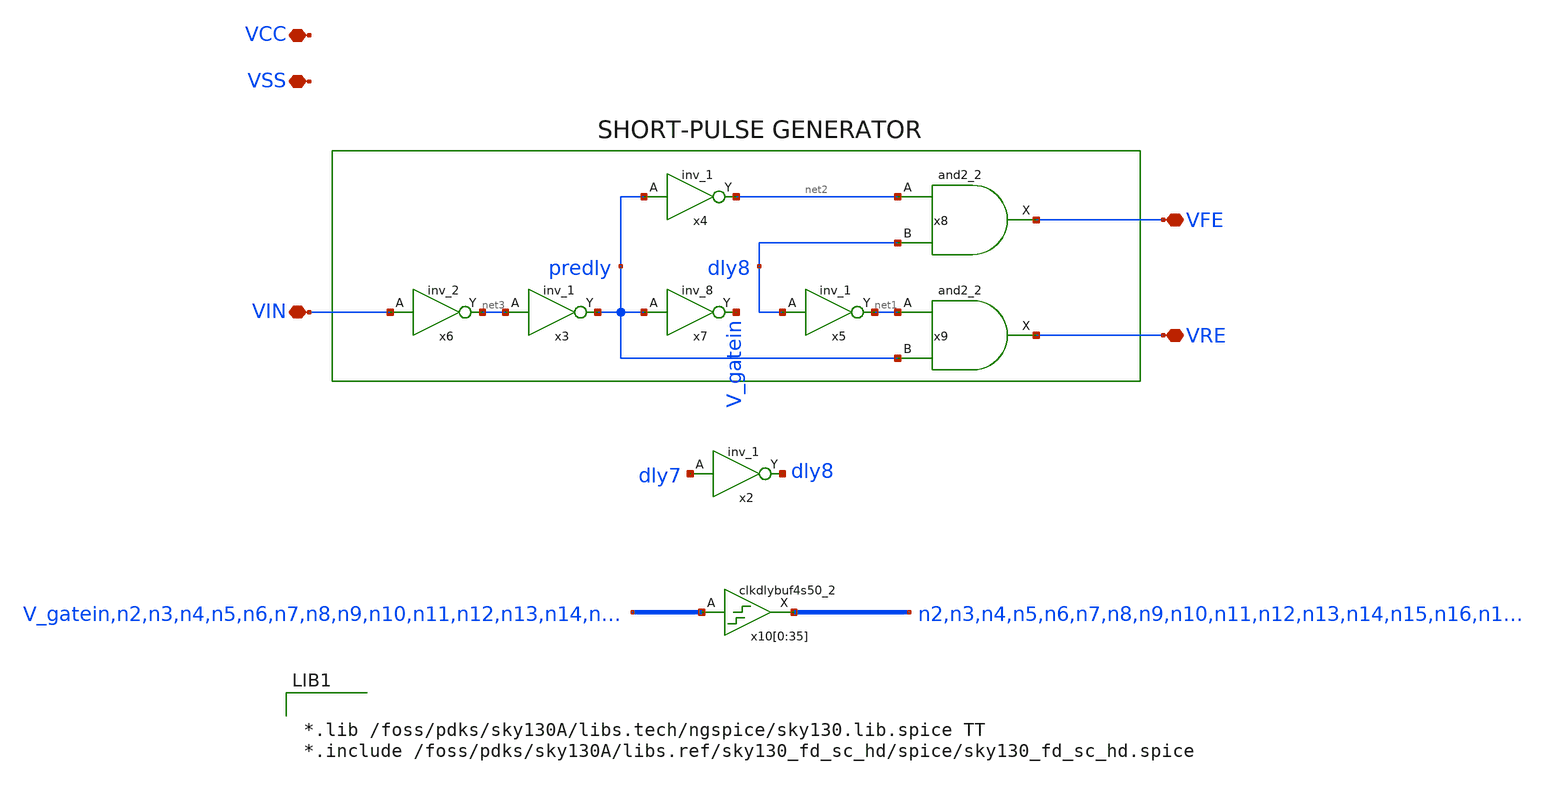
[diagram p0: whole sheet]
** sch_path: xschem/short_pulse_generator.sch
**.subckt short_pulse_generator VIN VFE VRE VCC VSS
*.iopin VIN
*.iopin VFE
*.iopin VRE
*.iopin VCC
*.iopin VSS
x3 net3 VSS VSS VCC VCC predly sky130_fd_sc_hd__inv_1
x4 predly VSS VSS VCC VCC net2 sky130_fd_sc_hd__inv_1
x5 dly8 VSS VSS VCC VCC net1 sky130_fd_sc_hd__inv_1
x6 VIN VSS VSS VCC VCC net3 sky130_fd_sc_hd__inv_2
x7 predly VSS VSS VCC VCC V_gatein sky130_fd_sc_hd__inv_8
x8 net2 dly8 VSS VSS VCC VCC VFE sky130_fd_sc_hd__and2_2
x9 net1 predly VSS VSS VCC VCC VRE sky130_fd_sc_hd__and2_2
x2 dly7 VSS VSS VCC VCC dly8 sky130_fd_sc_hd__inv_1
x10[0] V_gatein VSS VSS VCC VCC n2 sky130_fd_sc_hd__clkdlybuf4s50_2
x10[1] n2 VSS VSS VCC VCC n3 sky130_fd_sc_hd__clkdlybuf4s50_2
x10[2] n3 VSS VSS VCC VCC n4 sky130_fd_sc_hd__clkdlybuf4s50_2
x10[3] n4 VSS VSS VCC VCC n5 sky130_fd_sc_hd__clkdlybuf4s50_2
x10[4] n5 VSS VSS VCC VCC n6 sky130_fd_sc_hd__clkdlybuf4s50_2
x10[5] n6 VSS VSS VCC VCC n7 sky130_fd_sc_hd__clkdlybuf4s50_2
x10[6] n7 VSS VSS VCC VCC n8 sky130_fd_sc_hd__clkdlybuf4s50_2
x10[7] n8 VSS VSS VCC VCC n9 sky130_fd_sc_hd__clkdlybuf4s50_2
x10[8] n9 VSS VSS VCC VCC n10 sky130_fd_sc_hd__clkdlybuf4s50_2
x10[9] n10 VSS VSS VCC VCC n11 sky130_fd_sc_hd__clkdlybuf4s50_2
x10[10] n11 VSS VSS VCC VCC n12 sky130_fd_sc_hd__clkdlybuf4s50_2
x10[11] n12 VSS VSS VCC VCC n13 sky130_fd_sc_hd__clkdlybuf4s50_2
x10[12] n13 VSS VSS VCC VCC n14 sky130_fd_sc_hd__clkdlybuf4s50_2
x10[13] n14 VSS VSS VCC VCC n15 sky130_fd_sc_hd__clkdlybuf4s50_2
x10[14] n15 VSS VSS VCC VCC n16 sky130_fd_sc_hd__clkdlybuf4s50_2
x10[15] n16 VSS VSS VCC VCC n17 sky130_fd_sc_hd__clkdlybuf4s50_2
x10[16] n17 VSS VSS VCC VCC n18 sky130_fd_sc_hd__clkdlybuf4s50_2
x10[17] n18 VSS VSS VCC VCC n19 sky130_fd_sc_hd__clkdlybuf4s50_2
x10[18] n19 VSS VSS VCC VCC n20 sky130_fd_sc_hd__clkdlybuf4s50_2
x10[19] n20 VSS VSS VCC VCC n21 sky130_fd_sc_hd__clkdlybuf4s50_2
x10[20] n21 VSS VSS VCC VCC n22 sky130_fd_sc_hd__clkdlybuf4s50_2
x10[21] n22 VSS VSS VCC VCC n23 sky130_fd_sc_hd__clkdlybuf4s50_2
x10[22] n23 VSS VSS VCC VCC n24 sky130_fd_sc_hd__clkdlybuf4s50_2
x10[23] n24 VSS VSS VCC VCC n25 sky130_fd_sc_hd__clkdlybuf4s50_2
x10[24] n25 VSS VSS VCC VCC n26 sky130_fd_sc_hd__clkdlybuf4s50_2
x10[25] n26 VSS VSS VCC VCC n27 sky130_fd_sc_hd__clkdlybuf4s50_2
x10[26] n27 VSS VSS VCC VCC n28 sky130_fd_sc_hd__clkdlybuf4s50_2
x10[27] n28 VSS VSS VCC VCC n29 sky130_fd_sc_hd__clkdlybuf4s50_2
x10[28] n29 VSS VSS VCC VCC n30 sky130_fd_sc_hd__clkdlybuf4s50_2
x10[29] n30 VSS VSS VCC VCC n31 sky130_fd_sc_hd__clkdlybuf4s50_2
x10[30] n31 VSS VSS VCC VCC n32 sky130_fd_sc_hd__clkdlybuf4s50_2
x10[31] n32 VSS VSS VCC VCC n33 sky130_fd_sc_hd__clkdlybuf4s50_2
x10[32] n33 VSS VSS VCC VCC n34 sky130_fd_sc_hd__clkdlybuf4s50_2
x10[33] n34 VSS VSS VCC VCC n35 sky130_fd_sc_hd__clkdlybuf4s50_2
x10[34] n35 VSS VSS VCC VCC n36 sky130_fd_sc_hd__clkdlybuf4s50_2
x10[35] n36 VSS VSS VCC VCC dly7 sky130_fd_sc_hd__clkdlybuf4s50_2
**** begin user architecture code


*.lib /foss/pdks/sky130A/libs.tech/ngspice/sky130.lib.spice TT
*.include /foss/pdks/sky130A/libs.ref/sky130_fd_sc_hd/spice/sky130_fd_sc_hd.spice


**** end user architecture code
**.ends
.end
